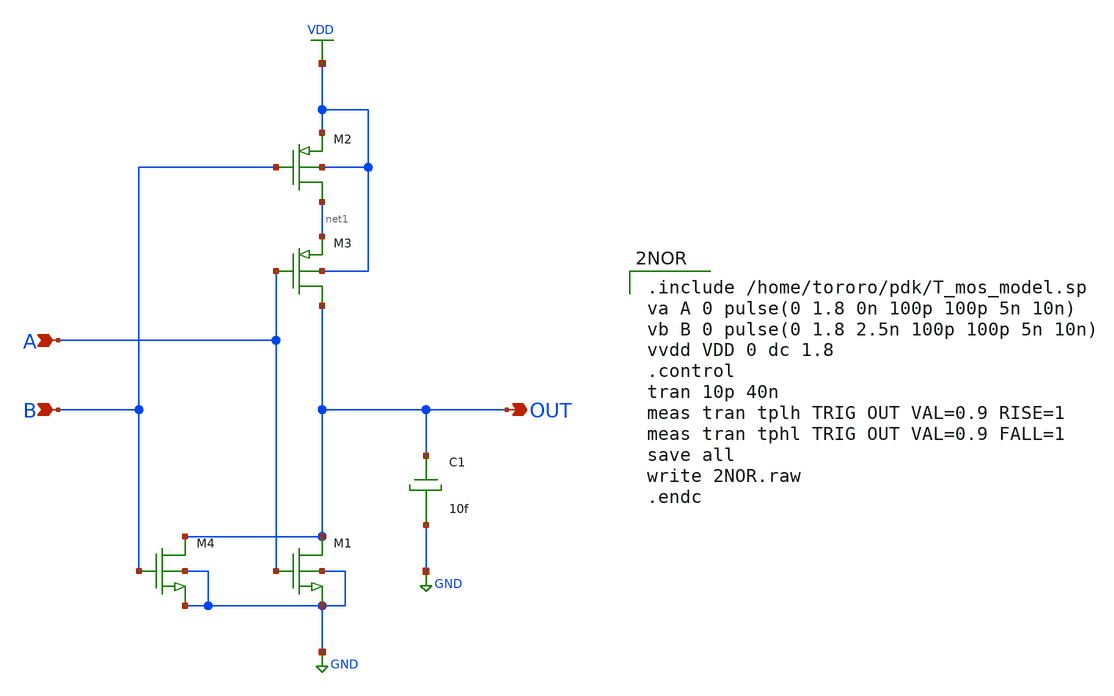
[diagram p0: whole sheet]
** sch_path: task1/2NOR.sch
**.subckt 2NOR OUT B A
*.opin OUT
*.ipin B
*.ipin A
M1 OUT A GND GND nch w=3.5u l=0.35u as=0 ps=0 ad=0 pd=0 m=1
M2 net1 B VDD VDD pch w=3.5u l=0.35u as=0 ps=0 ad=0 pd=0 m=1
M3 OUT A net1 VDD pch w=3.5u l=0.35u as=0 ps=0 ad=0 pd=0 m=1
M4 OUT B GND GND nch w=3.5u l=0.35u as=0 ps=0 ad=0 pd=0 m=1
C1 OUT GND 10f m=1
**** begin user architecture code

.include /home/tororo/pdk/T_mos_model.sp
va A 0 pulse(0 1.8 0n 100p 100p 5n 10n)
vb B 0 pulse(0 1.8 2.5n 100p 100p 5n 10n)
vvdd VDD 0 dc 1.8
.control
tran 10p 40n
meas tran tplh TRIG OUT VAL=0.9 RISE=1
meas tran tphl TRIG OUT VAL=0.9 FALL=1
save all
write 2NOR.raw
.endc

**** end user architecture code
**.ends
.GLOBAL VDD
.GLOBAL GND
.end
